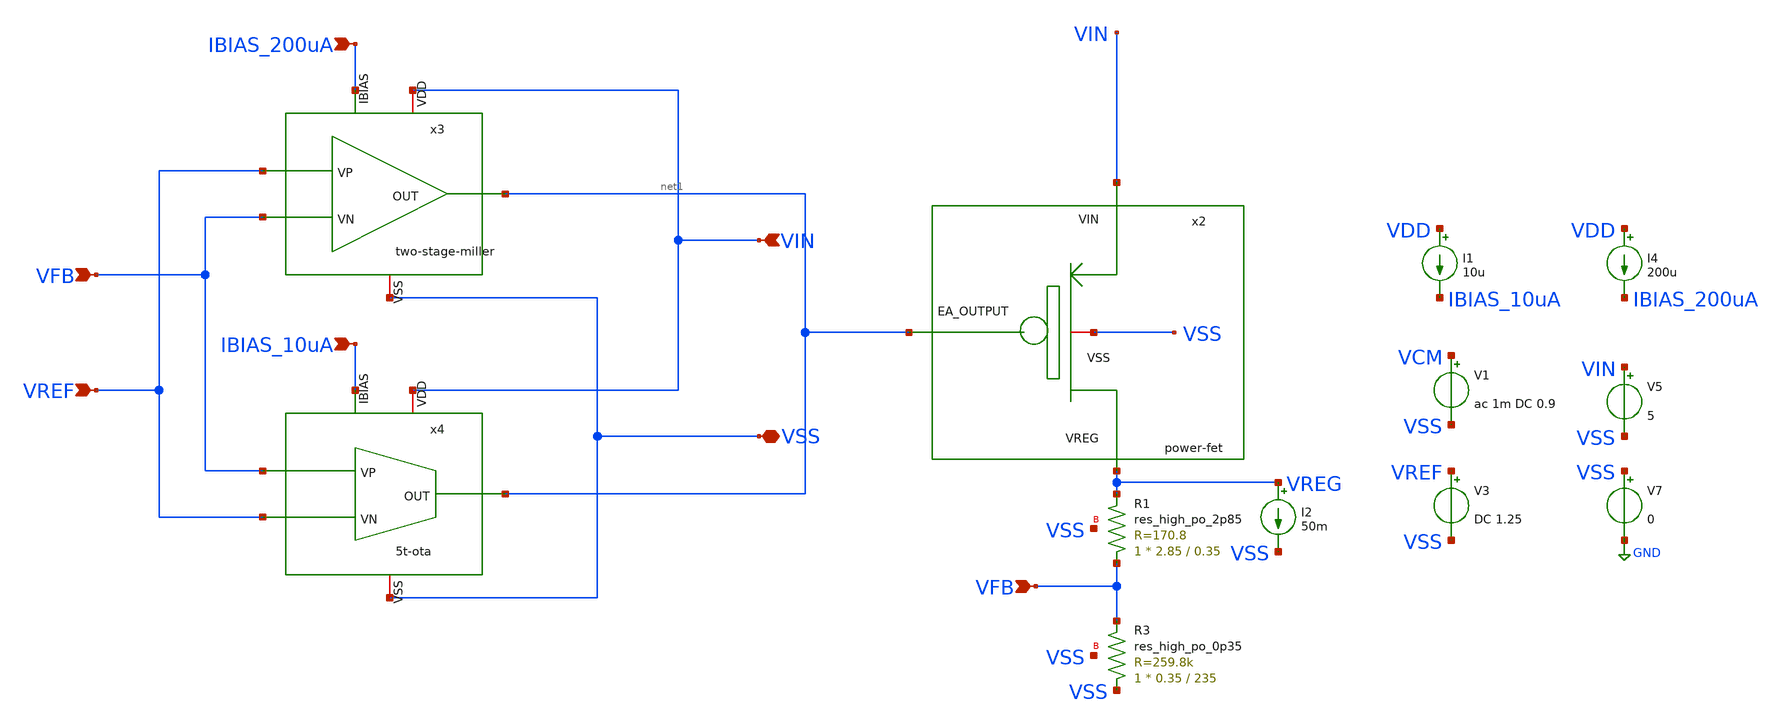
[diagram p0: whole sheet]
** sch_path: xschem/ldo-core/schematics/ldo-top.sch
**.subckt ldo-top VFB VFB VREF IBIAS_10uA IBIAS_200uA VIN VSS
*.ipin VFB
*.ipin VFB
*.ipin VREF
*.ipin IBIAS_10uA
*.ipin IBIAS_200uA
*.ipin VIN
*.iopin VSS
x2 VIN VSS net1 VREG power-fet
XR3 VSS VFB VSS sky130_fd_pr__res_high_po_0p35 L=235 mult=1 m=1
XR1 VFB VREG VSS sky130_fd_pr__res_high_po_2p85 L=0.35 mult=1 m=1
V3 VREF VSS DC 1.25
V5 VIN VSS 5
V7 VSS GND 0
I4 VDD IBIAS_200uA 200u
V1 VCM VSS ac 1m DC 0.9
I1 VDD IBIAS_10uA 10u
x3 VIN net1 VREF VFB IBIAS_200uA VSS two-stage-miller
x4 VIN net1 IBIAS_10uA VREF VFB VSS 5t-ota
I2 VREG VSS 50m
**** begin user architecture code
.lib $::SKYWATER_MODELS/sky130.lib.spice ss



.temp 27
.control

DC V5 0 5 0.01

* Nominal output voltage (from regulation region)
let Vout_nom = 1.25
let Vout_95  = 0.95*Vout_nom

* Find Vin where Vout crosses 95%
meas dc Vin_do find v(vin) when v(vreg)=Vout_95

* Measure Vout at that Vin (for completeness)
meas dc Vout_do find v(vreg) when v(vreg)=Vout_95

* Compute dropout voltage
let Vdo = Vin_do - Vout_do

print Vin_do Vout_do Vdo
plot VREG

.endc


**** end user architecture code
**.ends
.GLOBAL GND
.end
